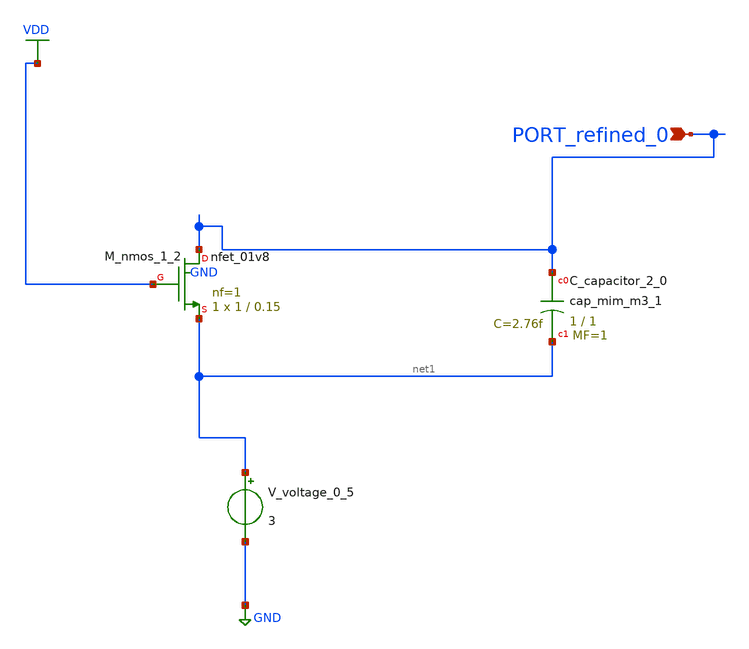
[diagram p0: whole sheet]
** sch_path: schematics/AMSNet/52.sch
**.subckt 52 PORT_refined_0
*.ipin PORT_refined_0
XC_capacitor_2_0 PORT_refined_0 net1 sky130_fd_pr__cap_mim_m3_1 W=1 L=1 MF=1 m=1
XM_nmos_1_2 PORT_refined_0 VDD net1 GND sky130_fd_pr__nfet_01v8 L=0.15 W=1 nf=1 ad='int((1 + 1)/2) * 1 / 1 * 0.29'
+ as='int((1 + 2)/2) * 1 / 1 * 0.29' pd='2*int((1 + 1)/2) * (1 / 1 + 0.29)' ps='2*int((1 + 2)/2) * (1 / 1 + 0.29)'
+ nrd='0.29 / 1 ' nrs='0.29 / 1 ' sa=0 sb=0 sd=0 mult=1 m=1
V_voltage_0_5 net1 GND 3
**.ends
.GLOBAL GND
.GLOBAL VDD
.end
